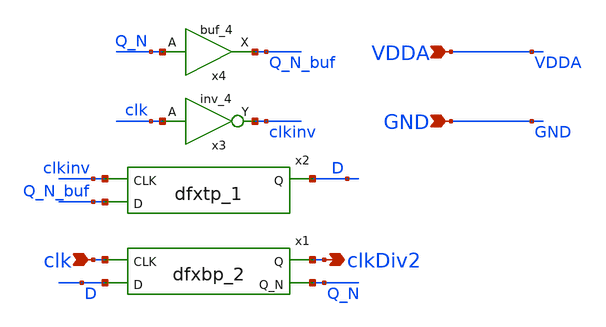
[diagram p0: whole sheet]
** sch_path: xschem/lib/DLib_freqDiv2.sch
**.subckt DLib_freqDiv2 clkDiv2 clk VDDA GND
*.opin clkDiv2
*.ipin clk
*.ipin VDDA
*.ipin GND
x1 clk D GND GND VDDA VDDA clkDiv2 Q_N sky130_fd_sc_hd__dfxbp_2
x2 clkinv Q_N_buf GND GND VDDA VDDA D sky130_fd_sc_hd__dfxtp_1
x3 clk GND GND VDDA VDDA clkinv sky130_fd_sc_hd__inv_4
x4 Q_N GND GND VDDA VDDA Q_N_buf sky130_fd_sc_hd__buf_4
**.ends
.end
